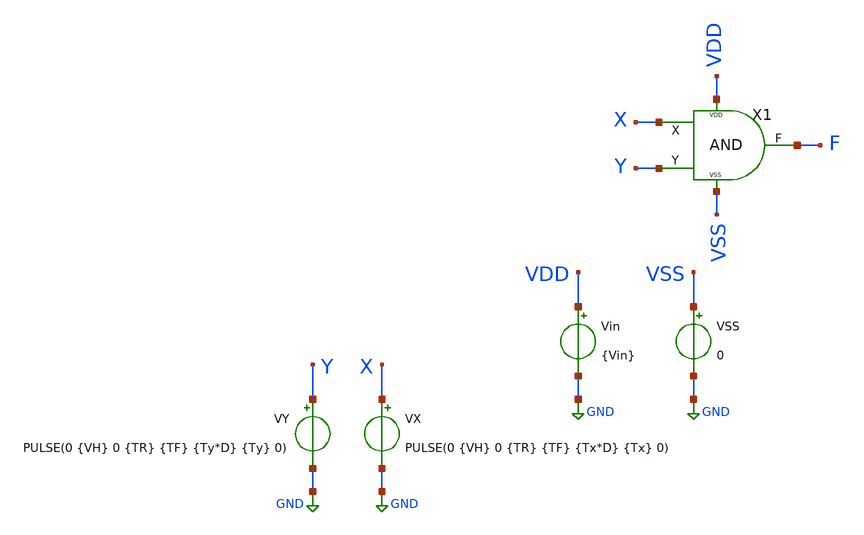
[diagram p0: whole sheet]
** sch_path: xschem/DigitalGates/TB_AND.sch
**.subckt TB_AND
Vin VDD GND {Vin}
VY Y GND PULSE(0 {VH} 0 {TR} {TF} {Ty*D} {Ty} 0)
VX X GND PULSE(0 {VH} 0 {TR} {TF} {Tx*D} {Tx} 0)
VSS VSS GND 0
X1 X Y VSS VDD F AND
**** begin user architecture code


.param Vin = 1.2
.param VH = 1.2
.param Del = 0

*.param fsw = 10Meg
*.param fsw = 8.4Meg
.param fsw = 1Meg

.param Tx = 1/fsw
.param Ty = Tx/5
.param D = 0.5
.param TR = 1n
.param TF = 1n
.param TdR = 0.5n
.param TdF = 0.5n

*.option temp = 125
*.option temp = -40
.option temp = 27





.save all
.param SimTime = 5*Tx
.csparam Sim_end = {SimTime}
*.csparam T = {T}

.tran 1n {SimTime} uic

.control
run
*meas tran P_M2_mean AVG P_M2 FROM={Tmeas_i} TO={Tmeas_end}

plot v(X) v(Y)+2 v(F)+4
*write TB_DCDCBuck.raw
.endc


.end




.param temp=27
.param mult = 1

.param w_P_AND =0.15u
.param l_P_AND = 0.15u

.param w_N_AND =0.15u
.param l_N_AND =0.15u








.lib cornerMOShv.lib mos_tt
.lib cornerMOSlv.lib mos_tt
*.lib cornerMOShv.lib mos_ff
*.lib cornerMOSlv.lib mos_ff
*.lib cornerMOShv.lib mos_ss
*.lib cornerMOSlv.lib mos_ss
*.lib cornerMOShv.lib mos_sf
*.lib cornerMOSlv.lib mos_sf
*.lib cornerMOShv.lib mos_fs
*.lib cornerMOSlv.lib mos_fs

*.include /opt/pdks/ihp-sg13g2/libs.ref/sg13g2_stdcell/spice/sg13g2_stdcell.spice
*.lib $::SG13G2_MODELS/cornerRES.lib res_typ
*.lib $::SG13G2_MODELS/cornerCAP.lib cap_typ
*.lib $::SG13G2_MODELS/diodes.lib




**** end user architecture code
**.ends

* expanding   symbol:  ../DigitalGates/AND.sym # of pins=5
** sym_path: xschem/DigitalGates/AND.sym
** sch_path: xschem/DigitalGates/AND.sch
.subckt AND X Y VSS VDD F
*.iopin VDD
*.ipin X
*.opin F
*.iopin VSS
*.ipin Y
XM1 net1 X net2 VSS sg13_lv_nmos w={w_N_AND} l={l_N_AND} ng=1 m={mult} mm_ok=1
XM2 F net1 VDD VDD sg13_lv_pmos w={w_P_AND} l={l_P_AND} ng=1 m={mult*3} mm_ok=1
XM3 net2 Y VSS VSS sg13_lv_nmos w={w_N_AND} l={l_N_AND} ng=1 m={mult} mm_ok=1
XM4 F net1 VSS VSS sg13_lv_nmos w={w_N_AND} l={l_N_AND} ng=1 m={mult} mm_ok=1
XM5 net1 Y VDD VDD sg13_lv_pmos w={w_P_AND} l={l_P_AND} ng=1 m={mult*3} mm_ok=1
XM6 net1 X VDD VDD sg13_lv_pmos w={w_P_AND} l={l_P_AND} ng=1 m={mult*3} mm_ok=1
**** begin user architecture code



**** end user architecture code
.ends

.GLOBAL GND
.end
